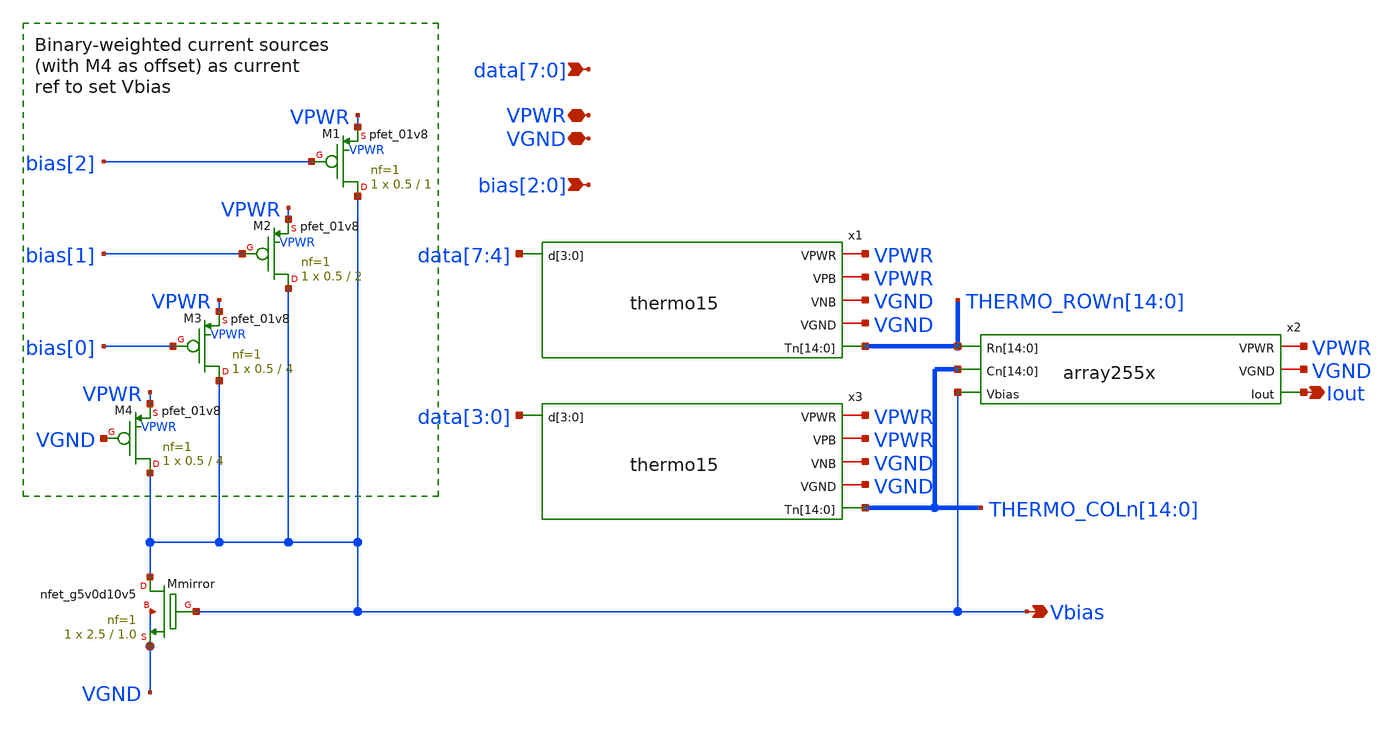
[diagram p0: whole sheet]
** sch_path: xschem/csdac255.sch
**.subckt csdac255 VPWR Iout VGND bias[2],bias[1],bias[0]
*+ data[7],data[6],data[5],data[4],data[3],data[2],data[1],data[0] Vbias
*.iopin VPWR
*.opin Iout
*.iopin VGND
*.ipin bias[2],bias[1],bias[0]
*.ipin data[7],data[6],data[5],data[4],data[3],data[2],data[1],data[0]
*.opin Vbias
x1 VPWR VGND VPWR VGND THERMO_ROWn[14] THERMO_ROWn[13] THERMO_ROWn[12] THERMO_ROWn[11]
+ THERMO_ROWn[10] THERMO_ROWn[9] THERMO_ROWn[8] THERMO_ROWn[7] THERMO_ROWn[6] THERMO_ROWn[5] THERMO_ROWn[4]
+ THERMO_ROWn[3] THERMO_ROWn[2] THERMO_ROWn[1] THERMO_ROWn[0] data[7] data[6] data[5] data[4] thermo15
x2 VPWR VGND THERMO_ROWn[14] THERMO_ROWn[13] THERMO_ROWn[12] THERMO_ROWn[11] THERMO_ROWn[10]
+ THERMO_ROWn[9] THERMO_ROWn[8] THERMO_ROWn[7] THERMO_ROWn[6] THERMO_ROWn[5] THERMO_ROWn[4] THERMO_ROWn[3]
+ THERMO_ROWn[2] THERMO_ROWn[1] THERMO_ROWn[0] THERMO_COLn[14] THERMO_COLn[13] THERMO_COLn[12] THERMO_COLn[11]
+ THERMO_COLn[10] THERMO_COLn[9] THERMO_COLn[8] THERMO_COLn[7] THERMO_COLn[6] THERMO_COLn[5] THERMO_COLn[4]
+ THERMO_COLn[3] THERMO_COLn[2] THERMO_COLn[1] THERMO_COLn[0] Vbias Iout array255x
x3 VPWR VGND VPWR VGND THERMO_COLn[14] THERMO_COLn[13] THERMO_COLn[12] THERMO_COLn[11]
+ THERMO_COLn[10] THERMO_COLn[9] THERMO_COLn[8] THERMO_COLn[7] THERMO_COLn[6] THERMO_COLn[5] THERMO_COLn[4]
+ THERMO_COLn[3] THERMO_COLn[2] THERMO_COLn[1] THERMO_COLn[0] data[3] data[2] data[1] data[0] thermo15
XM1 Vbias bias[2] VPWR VPWR sky130_fd_pr__pfet_01v8 L=1 W=0.5 nf=1 ad='int((nf+1)/2) * W/nf * 0.29' as='int((nf+2)/2) * W/nf * 0.29'
+ pd='2*int((nf+1)/2) * (W/nf + 0.29)' ps='2*int((nf+2)/2) * (W/nf + 0.29)' nrd='0.29 / W' nrs='0.29 / W'
+ sa=0 sb=0 sd=0 mult=1 m=1
XM2 Vbias bias[1] VPWR VPWR sky130_fd_pr__pfet_01v8 L=2 W=0.5 nf=1 ad='int((nf+1)/2) * W/nf * 0.29' as='int((nf+2)/2) * W/nf * 0.29'
+ pd='2*int((nf+1)/2) * (W/nf + 0.29)' ps='2*int((nf+2)/2) * (W/nf + 0.29)' nrd='0.29 / W' nrs='0.29 / W'
+ sa=0 sb=0 sd=0 mult=1 m=1
XM3 Vbias bias[0] VPWR VPWR sky130_fd_pr__pfet_01v8 L=4 W=0.5 nf=1 ad='int((nf+1)/2) * W/nf * 0.29' as='int((nf+2)/2) * W/nf * 0.29'
+ pd='2*int((nf+1)/2) * (W/nf + 0.29)' ps='2*int((nf+2)/2) * (W/nf + 0.29)' nrd='0.29 / W' nrs='0.29 / W'
+ sa=0 sb=0 sd=0 mult=1 m=1
XMmirror Vbias Vbias VGND VGND sky130_fd_pr__nfet_g5v0d10v5 L=1.0 W=2.5 nf=1 ad='int((nf+1)/2) * W/nf * 0.29'
+ as='int((nf+2)/2) * W/nf * 0.29' pd='2*int((nf+1)/2) * (W/nf + 0.29)' ps='2*int((nf+2)/2) * (W/nf + 0.29)'
+ nrd='0.29 / W' nrs='0.29 / W' sa=0 sb=0 sd=0 mult=1 m=1
XM4 Vbias VGND VPWR VPWR sky130_fd_pr__pfet_01v8 L=4 W=0.5 nf=1 ad='int((nf+1)/2) * W/nf * 0.29' as='int((nf+2)/2) * W/nf * 0.29'
+ pd='2*int((nf+1)/2) * (W/nf + 0.29)' ps='2*int((nf+2)/2) * (W/nf + 0.29)' nrd='0.29 / W' nrs='0.29 / W'
+ sa=0 sb=0 sd=0 mult=1 m=1
**.ends

* expanding   symbol:  thermo15.sym # of pins=6
** sym_path: xschem/thermo15.sym
** sch_path: xschem/thermo15.sch
.subckt thermo15 VPWR VGND VPB VNB Tn[14] Tn[13] Tn[12] Tn[11] Tn[10] Tn[9] Tn[8] Tn[7] Tn[6] Tn[5]
+ Tn[4] Tn[3] Tn[2] Tn[1] Tn[0] d[3] d[2] d[1] d[0]
*.iopin VPWR
*.ipin d[3],d[2],d[1],d[0]
*.iopin VGND
*.iopin VPB
*.iopin VNB
*.opin
*+ Tn[14],Tn[13],Tn[12],Tn[11],Tn[10],Tn[9],Tn[8],Tn[7],Tn[6],Tn[5],Tn[4],Tn[3],Tn[2],Tn[1],Tn[0]
x1 d[1] VGND VNB VPB VPWR net3 sky130_fd_sc_hd__inv_1
x2 net5 VGND VNB VPB VPWR net6 sky130_fd_sc_hd__inv_2
x3 d[0] d[1] VGND VNB VPB VPWR net4 sky130_fd_sc_hd__nand2_1
x4 d[0] d[1] VGND VNB VPB VPWR net2 sky130_fd_sc_hd__nor2_1
x5 d[2] VGND VNB VPB VPWR net1 sky130_fd_sc_hd__inv_1
x6 net2 net1 VGND VNB VPB VPWR net7 sky130_fd_sc_hd__nand2_1
x7 net3 net1 VGND VNB VPB VPWR net8 sky130_fd_sc_hd__nand2_1
x8 net4 net1 VGND VNB VPB VPWR net9 sky130_fd_sc_hd__nand2_1
x9 net1 VGND VNB VPB VPWR net10 sky130_fd_sc_hd__inv_1
x10 net2 net1 VGND VNB VPB VPWR net11 sky130_fd_sc_hd__nor2_1
x11 net3 net1 VGND VNB VPB VPWR net12 sky130_fd_sc_hd__nor2_1
x12 net4 net1 VGND VNB VPB VPWR net13 sky130_fd_sc_hd__nor2_1
x13 net7 net6 VGND VNB VPB VPWR Tn[0] sky130_fd_sc_hd__nor2_4
x14 net8 net6 VGND VNB VPB VPWR Tn[1] sky130_fd_sc_hd__nor2_4
x15 net9 net6 VGND VNB VPB VPWR Tn[2] sky130_fd_sc_hd__nor2_4
x16 net10 net6 VGND VNB VPB VPWR Tn[3] sky130_fd_sc_hd__nor2_4
x17 net11 net6 VGND VNB VPB VPWR Tn[4] sky130_fd_sc_hd__nor2_4
x18 net12 net6 VGND VNB VPB VPWR Tn[5] sky130_fd_sc_hd__nor2_4
x19 net13 net6 VGND VNB VPB VPWR Tn[6] sky130_fd_sc_hd__nor2_4
x20 net6 VGND VNB VPB VPWR Tn[7] sky130_fd_sc_hd__inv_4
x21 net7 net6 VGND VNB VPB VPWR Tn[8] sky130_fd_sc_hd__nand2_4
x22 net8 net6 VGND VNB VPB VPWR Tn[9] sky130_fd_sc_hd__nand2_4
x23 net9 net6 VGND VNB VPB VPWR Tn[10] sky130_fd_sc_hd__nand2_4
x24 net10 net6 VGND VNB VPB VPWR Tn[11] sky130_fd_sc_hd__nand2_4
x25 net11 net6 VGND VNB VPB VPWR Tn[12] sky130_fd_sc_hd__nand2_4
x26 net12 net6 VGND VNB VPB VPWR Tn[13] sky130_fd_sc_hd__nand2_4
x27 net13 net6 VGND VNB VPB VPWR Tn[14] sky130_fd_sc_hd__nand2_4
x28 d[3] VGND VNB VPB VPWR net5 sky130_fd_sc_hd__inv_1
.ends


* expanding   symbol:  array255x.sym # of pins=6
** sym_path: xschem/array255x.sym
** sch_path: xschem/array255x.sch
.subckt array255x VPWR VGND Rn[14] Rn[13] Rn[12] Rn[11] Rn[10] Rn[9] Rn[8] Rn[7] Rn[6] Rn[5] Rn[4]
+ Rn[3] Rn[2] Rn[1] Rn[0] Cn[14] Cn[13] Cn[12] Cn[11] Cn[10] Cn[9] Cn[8] Cn[7] Cn[6] Cn[5] Cn[4] Cn[3]
+ Cn[2] Cn[1] Cn[0] Vbias Iout
*.iopin VPWR
*.opin Iout
*.iopin VGND
*.ipin Vbias
*.ipin
*+ Cn[14],Cn[13],Cn[12],Cn[11],Cn[10],Cn[9],Cn[8],Cn[7],Cn[6],Cn[5],Cn[4],Cn[3],Cn[2],Cn[1],Cn[0]
*.ipin
*+ Rn[14],Rn[13],Rn[12],Rn[11],Rn[10],Rn[9],Rn[8],Rn[7],Rn[6],Rn[5],Rn[4],Rn[3],Rn[2],Rn[1],Rn[0]
XIR[14] Vbias VPWR Rn[14] Rn[13] Cn[14] Cn[13] Cn[12] Cn[11] Cn[10] Cn[9] Cn[8] Cn[7] Cn[6] Cn[5]
+ Cn[4] Cn[3] Cn[2] Cn[1] Cn[0] VGND Iout row15x
XIR[13] Vbias VPWR Rn[13] Rn[12] Cn[14] Cn[13] Cn[12] Cn[11] Cn[10] Cn[9] Cn[8] Cn[7] Cn[6] Cn[5]
+ Cn[4] Cn[3] Cn[2] Cn[1] Cn[0] VGND Iout row15x
XIR[12] Vbias VPWR Rn[12] Rn[11] Cn[14] Cn[13] Cn[12] Cn[11] Cn[10] Cn[9] Cn[8] Cn[7] Cn[6] Cn[5]
+ Cn[4] Cn[3] Cn[2] Cn[1] Cn[0] VGND Iout row15x
XIR[11] Vbias VPWR Rn[11] Rn[10] Cn[14] Cn[13] Cn[12] Cn[11] Cn[10] Cn[9] Cn[8] Cn[7] Cn[6] Cn[5]
+ Cn[4] Cn[3] Cn[2] Cn[1] Cn[0] VGND Iout row15x
XIR[10] Vbias VPWR Rn[10] Rn[9] Cn[14] Cn[13] Cn[12] Cn[11] Cn[10] Cn[9] Cn[8] Cn[7] Cn[6] Cn[5]
+ Cn[4] Cn[3] Cn[2] Cn[1] Cn[0] VGND Iout row15x
XIR[9] Vbias VPWR Rn[9] Rn[8] Cn[14] Cn[13] Cn[12] Cn[11] Cn[10] Cn[9] Cn[8] Cn[7] Cn[6] Cn[5] Cn[4]
+ Cn[3] Cn[2] Cn[1] Cn[0] VGND Iout row15x
XIR[8] Vbias VPWR Rn[8] Rn[7] Cn[14] Cn[13] Cn[12] Cn[11] Cn[10] Cn[9] Cn[8] Cn[7] Cn[6] Cn[5] Cn[4]
+ Cn[3] Cn[2] Cn[1] Cn[0] VGND Iout row15x
XIR[7] Vbias VPWR Rn[7] Rn[6] Cn[14] Cn[13] Cn[12] Cn[11] Cn[10] Cn[9] Cn[8] Cn[7] Cn[6] Cn[5] Cn[4]
+ Cn[3] Cn[2] Cn[1] Cn[0] VGND Iout row15x
XIR[6] Vbias VPWR Rn[6] Rn[5] Cn[14] Cn[13] Cn[12] Cn[11] Cn[10] Cn[9] Cn[8] Cn[7] Cn[6] Cn[5] Cn[4]
+ Cn[3] Cn[2] Cn[1] Cn[0] VGND Iout row15x
XIR[5] Vbias VPWR Rn[5] Rn[4] Cn[14] Cn[13] Cn[12] Cn[11] Cn[10] Cn[9] Cn[8] Cn[7] Cn[6] Cn[5] Cn[4]
+ Cn[3] Cn[2] Cn[1] Cn[0] VGND Iout row15x
XIR[4] Vbias VPWR Rn[4] Rn[3] Cn[14] Cn[13] Cn[12] Cn[11] Cn[10] Cn[9] Cn[8] Cn[7] Cn[6] Cn[5] Cn[4]
+ Cn[3] Cn[2] Cn[1] Cn[0] VGND Iout row15x
XIR[3] Vbias VPWR Rn[3] Rn[2] Cn[14] Cn[13] Cn[12] Cn[11] Cn[10] Cn[9] Cn[8] Cn[7] Cn[6] Cn[5] Cn[4]
+ Cn[3] Cn[2] Cn[1] Cn[0] VGND Iout row15x
XIR[2] Vbias VPWR Rn[2] Rn[1] Cn[14] Cn[13] Cn[12] Cn[11] Cn[10] Cn[9] Cn[8] Cn[7] Cn[6] Cn[5] Cn[4]
+ Cn[3] Cn[2] Cn[1] Cn[0] VGND Iout row15x
XIR[1] Vbias VPWR Rn[1] Rn[0] Cn[14] Cn[13] Cn[12] Cn[11] Cn[10] Cn[9] Cn[8] Cn[7] Cn[6] Cn[5] Cn[4]
+ Cn[3] Cn[2] Cn[1] Cn[0] VGND Iout row15x
XIR[0] Vbias VPWR Rn[0] VGND Cn[14] Cn[13] Cn[12] Cn[11] Cn[10] Cn[9] Cn[8] Cn[7] Cn[6] Cn[5] Cn[4]
+ Cn[3] Cn[2] Cn[1] Cn[0] VGND Iout row15x
XIR[15] Vbias VPWR VPWR Rn[14] Cn[14] Cn[13] Cn[12] Cn[11] Cn[10] Cn[9] Cn[8] Cn[7] Cn[6] Cn[5]
+ Cn[4] Cn[3] Cn[2] Cn[1] Cn[0] VGND Iout row15x
.ends


* expanding   symbol:  row15x.sym # of pins=7
** sym_path: xschem/row15x.sym
** sch_path: xschem/row15x.sch
.subckt row15x Vbias VPWR Sn Rn Cn[14] Cn[13] Cn[12] Cn[11] Cn[10] Cn[9] Cn[8] Cn[7] Cn[6] Cn[5]
+ Cn[4] Cn[3] Cn[2] Cn[1] Cn[0] VGND Iout
*.ipin Sn
*.ipin Rn
*.ipin
*+ Cn[14],Cn[13],Cn[12],Cn[11],Cn[10],Cn[9],Cn[8],Cn[7],Cn[6],Cn[5],Cn[4],Cn[3],Cn[2],Cn[1],Cn[0]
*.iopin VPWR
*.iopin VGND
*.opin Iout
*.ipin Vbias
XIC[14] VPWR VGND Rn Cn[14] Sn Vbias Iout icell
XIC[13] VPWR VGND Rn Cn[13] Sn Vbias Iout icell
XIC[12] VPWR VGND Rn Cn[12] Sn Vbias Iout icell
XIC[11] VPWR VGND Rn Cn[11] Sn Vbias Iout icell
XIC[10] VPWR VGND Rn Cn[10] Sn Vbias Iout icell
XIC[9] VPWR VGND Rn Cn[9] Sn Vbias Iout icell
XIC[8] VPWR VGND Rn Cn[8] Sn Vbias Iout icell
XIC[7] VPWR VGND Rn Cn[7] Sn Vbias Iout icell
XIC[6] VPWR VGND Rn Cn[6] Sn Vbias Iout icell
XIC[5] VPWR VGND Rn Cn[5] Sn Vbias Iout icell
XIC[4] VPWR VGND Rn Cn[4] Sn Vbias Iout icell
XIC[3] VPWR VGND Rn Cn[3] Sn Vbias Iout icell
XIC[2] VPWR VGND Rn Cn[2] Sn Vbias Iout icell
XIC[1] VPWR VGND Rn Cn[1] Sn Vbias Iout icell
XIC[0] VPWR VGND Rn Cn[0] Sn Vbias Iout icell
XIC[15] VPWR VGND VPWR VPWR Sn Vbias Iout icell
XIC_dummy_left VPWR VGND VPWR VPWR VPWR VGND net1 icell
XIC_dummy_right VPWR VGND VPWR VPWR VPWR VGND net2 icell
.ends


* expanding   symbol:  icell.sym # of pins=7
** sym_path: xschem/icell.sym
** sch_path: xschem/icell.sch
.subckt icell VPWR VGND Rn Cn Sn Vbias Iout
*.ipin Rn
*.iopin VPWR
*.opin Iout
*.iopin VGND
*.ipin Cn
*.ipin Sn
*.ipin Vbias
XMsp Ien Sn VPWR VPWR sky130_fd_pr__pfet_01v8 L=0.15 W=0.5 nf=1 ad='int((nf+1)/2) * W/nf * 0.29' as='int((nf+2)/2) * W/nf * 0.29'
+ pd='2*int((nf+1)/2) * (W/nf + 0.29)' ps='2*int((nf+2)/2) * (W/nf + 0.29)' nrd='0.29 / W' nrs='0.29 / W'
+ sa=0 sb=0 sd=0 mult=1 m=1
XMsna Ien Sn PDM VGND sky130_fd_pr__nfet_01v8 L=0.15 W=0.5 nf=1 ad='int((nf+1)/2) * W/nf * 0.29' as='int((nf+2)/2) * W/nf * 0.29'
+ pd='2*int((nf+1)/2) * (W/nf + 0.29)' ps='2*int((nf+2)/2) * (W/nf + 0.29)' nrd='0.29 / W' nrs='0.29 / W'
+ sa=0 sb=0 sd=0 mult=1 m=1
XMcpa Ien Cn PUM VPWR sky130_fd_pr__pfet_01v8 L=0.15 W=0.5 nf=1 ad='int((nf+1)/2) * W/nf * 0.29' as='int((nf+2)/2) * W/nf * 0.29'
+ pd='2*int((nf+1)/2) * (W/nf + 0.29)' ps='2*int((nf+2)/2) * (W/nf + 0.29)' nrd='0.29 / W' nrs='0.29 / W'
+ sa=0 sb=0 sd=0 mult=1 m=1
XMrpa PUM Rn VPWR VPWR sky130_fd_pr__pfet_01v8 L=0.15 W=0.5 nf=1 ad='int((nf+1)/2) * W/nf * 0.29' as='int((nf+2)/2) * W/nf * 0.29'
+ pd='2*int((nf+1)/2) * (W/nf + 0.29)' ps='2*int((nf+2)/2) * (W/nf + 0.29)' nrd='0.29 / W' nrs='0.29 / W'
+ sa=0 sb=0 sd=0 mult=1 m=1
XMrno PDM Rn VGND VGND sky130_fd_pr__nfet_01v8 L=0.15 W=0.5 nf=1 ad='int((nf+1)/2) * W/nf * 0.29' as='int((nf+2)/2) * W/nf * 0.29'
+ pd='2*int((nf+1)/2) * (W/nf + 0.29)' ps='2*int((nf+2)/2) * (W/nf + 0.29)' nrd='0.29 / W' nrs='0.29 / W'
+ sa=0 sb=0 sd=0 mult=1 m=1
XMcno PDM Cn VGND VGND sky130_fd_pr__nfet_01v8 L=0.15 W=0.5 nf=1 ad='int((nf+1)/2) * W/nf * 0.29' as='int((nf+2)/2) * W/nf * 0.29'
+ pd='2*int((nf+1)/2) * (W/nf + 0.29)' ps='2*int((nf+2)/2) * (W/nf + 0.29)' nrd='0.29 / W' nrs='0.29 / W'
+ sa=0 sb=0 sd=0 mult=1 m=1
XMiu SM Vbias VGND VGND sky130_fd_pr__nfet_g5v0d10v5 L=0.5 W=0.5 nf=1 ad='int((nf+1)/2) * W/nf * 0.29'
+ as='int((nf+2)/2) * W/nf * 0.29' pd='2*int((nf+1)/2) * (W/nf + 0.29)' ps='2*int((nf+2)/2) * (W/nf + 0.29)'
+ nrd='0.29 / W' nrs='0.29 / W' sa=0 sb=0 sd=0 mult=1 m=1
XMsw Iout Ien SM VGND sky130_fd_pr__nfet_g5v0d10v5 L=0.5 W=0.5 nf=1 ad='int((nf+1)/2) * W/nf * 0.29'
+ as='int((nf+2)/2) * W/nf * 0.29' pd='2*int((nf+1)/2) * (W/nf + 0.29)' ps='2*int((nf+2)/2) * (W/nf + 0.29)'
+ nrd='0.29 / W' nrs='0.29 / W' sa=0 sb=0 sd=0 mult=1 m=1
.ends

.end
